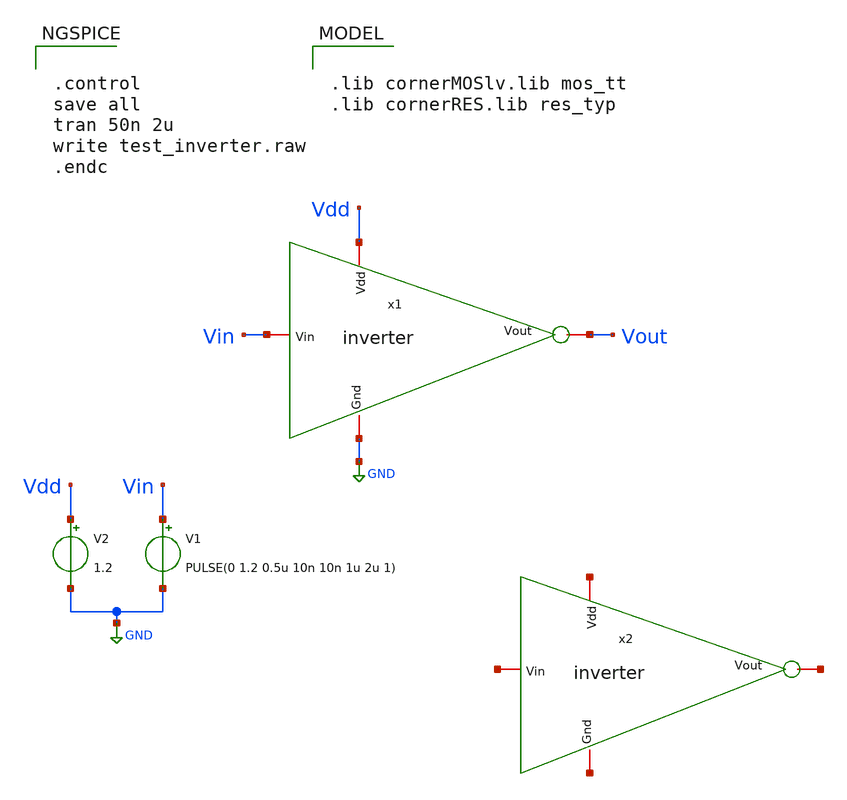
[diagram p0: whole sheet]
** sch_path: modules/module_0_foundations/inverter_example/inverter_tb.sch
**.subckt inverter_tb
V1 Vin GND PULSE(0 1.2 0.5u 10n 10n 1u 2u 1)
V2 Vdd GND 1.2
x1 Vdd Vin Vout GND inverter
x2 net1 net2 net3 net4 inverter
**** begin user architecture code


.control
save all
tran 50n 2u
write test_inverter.raw
.endc



.lib cornerMOSlv.lib mos_tt
.lib cornerRES.lib res_typ


**** end user architecture code
**.ends
.GLOBAL GND
.end
